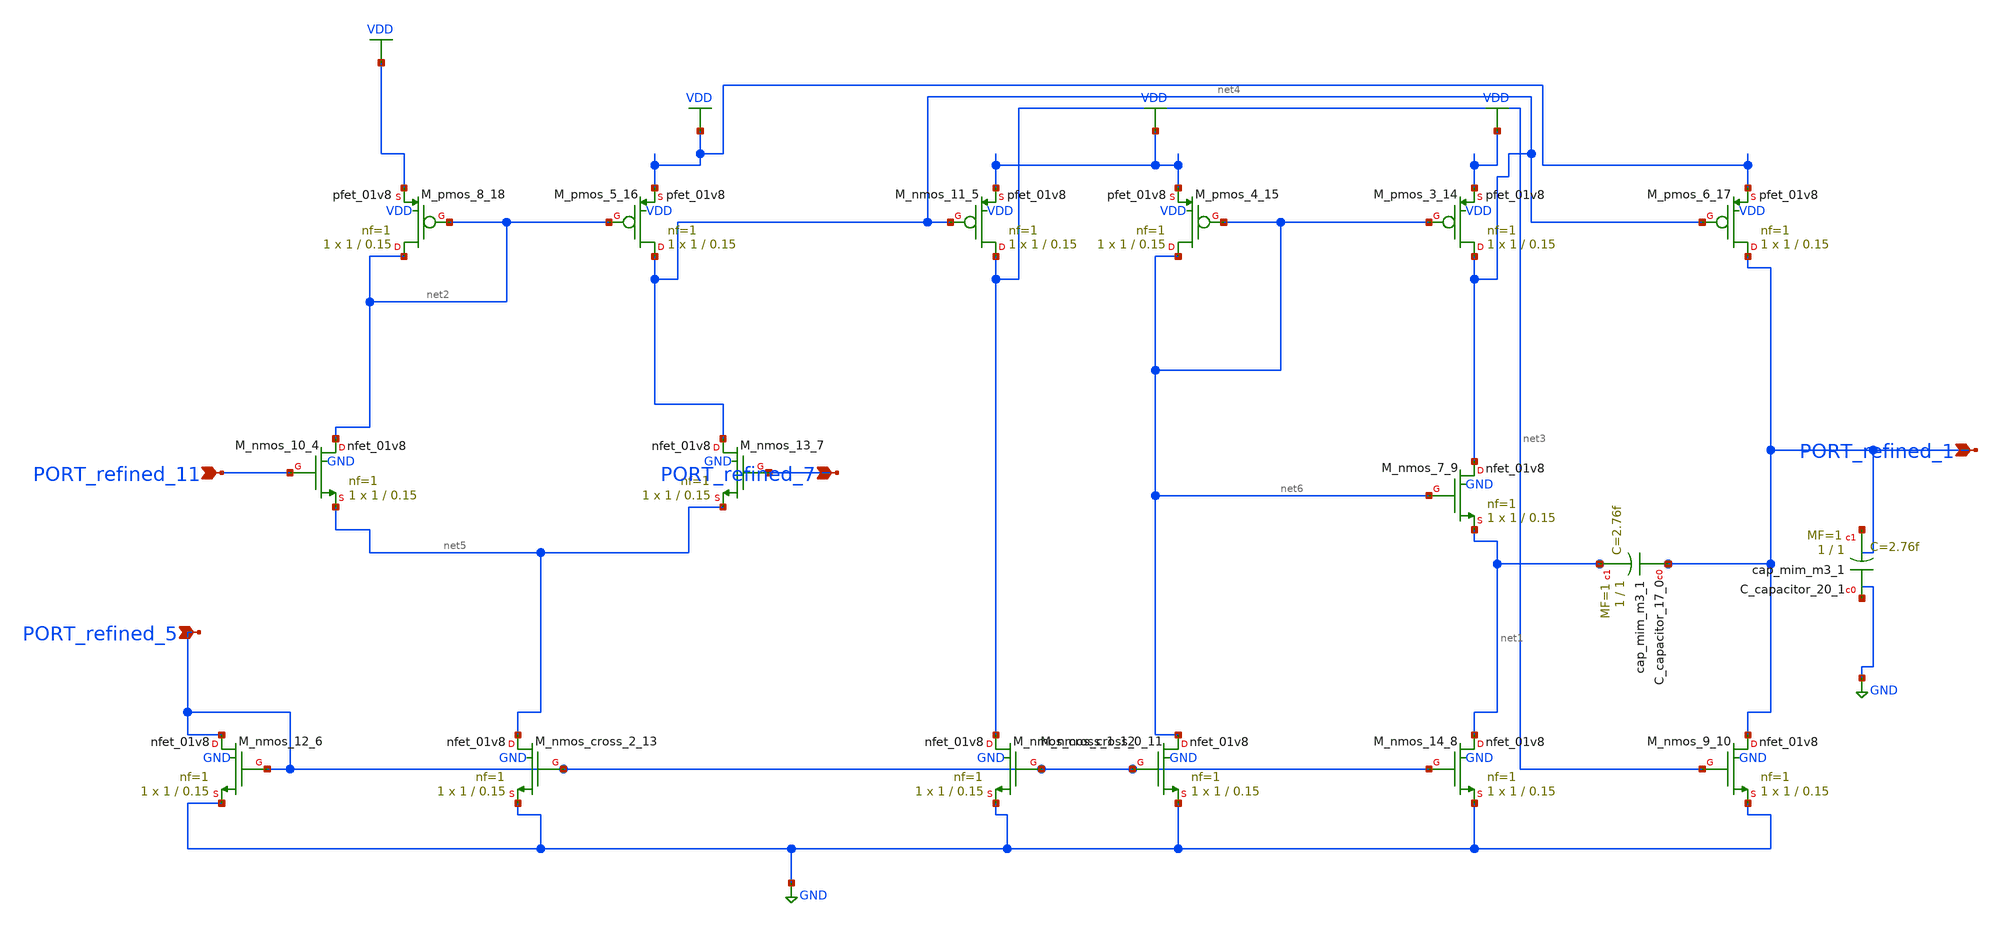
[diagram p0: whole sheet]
** sch_path: schematics/Image2Net/080.sch
**.subckt 080 PORT_refined_7 PORT_refined_11 PORT_refined_1 PORT_refined_5
*.ipin PORT_refined_7
*.ipin PORT_refined_11
*.ipin PORT_refined_1
*.ipin PORT_refined_5
XC_capacitor_17_0 PORT_refined_1 net1 sky130_fd_pr__cap_mim_m3_1 W=1 L=1 MF=1 m=1
XC_capacitor_20_1 GND PORT_refined_1 sky130_fd_pr__cap_mim_m3_1 W=1 L=1 MF=1 m=1
XM_nmos_10_4 net2 PORT_refined_11 net5 GND sky130_fd_pr__nfet_01v8 L=0.15 W=1 nf=1 ad='int((1 + 1)/2) * 1 / 1 * 0.29'
+ as='int((1 + 2)/2) * 1 / 1 * 0.29' pd='2*int((1 + 1)/2) * (1 / 1 + 0.29)' ps='2*int((1 + 2)/2) * (1 / 1 + 0.29)'
+ nrd='0.29 / 1 ' nrs='0.29 / 1 ' sa=0 sb=0 sd=0 mult=1 m=1
XM_nmos_11_5 net3 net4 VDD VDD sky130_fd_pr__pfet_01v8 L=0.15 W=1 nf=1 ad='int((1 + 1)/2) * 1 / 1 * 0.29'
+ as='int((1 + 2)/2) * 1 / 1 * 0.29' pd='2*int((1 + 1)/2) * (1 / 1 + 0.29)' ps='2*int((1 + 2)/2) * (1 / 1 + 0.29)'
+ nrd='0.29 / 1 ' nrs='0.29 / 1 ' sa=0 sb=0 sd=0 mult=1 m=1
XM_nmos_12_6 PORT_refined_5 PORT_refined_5 GND GND sky130_fd_pr__nfet_01v8 L=0.15 W=1 nf=1 ad='int((1 + 1)/2) * 1 / 1 * 0.29'
+ as='int((1 + 2)/2) * 1 / 1 * 0.29' pd='2*int((1 + 1)/2) * (1 / 1 + 0.29)' ps='2*int((1 + 2)/2) * (1 / 1 + 0.29)'
+ nrd='0.29 / 1 ' nrs='0.29 / 1 ' sa=0 sb=0 sd=0 mult=1 m=1
XM_nmos_13_7 net4 PORT_refined_7 net5 GND sky130_fd_pr__nfet_01v8 L=0.15 W=1 nf=1 ad='int((1 + 1)/2) * 1 / 1 * 0.29'
+ as='int((1 + 2)/2) * 1 / 1 * 0.29' pd='2*int((1 + 1)/2) * (1 / 1 + 0.29)' ps='2*int((1 + 2)/2) * (1 / 1 + 0.29)'
+ nrd='0.29 / 1 ' nrs='0.29 / 1 ' sa=0 sb=0 sd=0 mult=1 m=1
XM_nmos_14_8 net1 PORT_refined_5 GND GND sky130_fd_pr__nfet_01v8 L=0.15 W=1 nf=1 ad='int((1 + 1)/2) * 1 / 1 * 0.29'
+ as='int((1 + 2)/2) * 1 / 1 * 0.29' pd='2*int((1 + 1)/2) * (1 / 1 + 0.29)' ps='2*int((1 + 2)/2) * (1 / 1 + 0.29)'
+ nrd='0.29 / 1 ' nrs='0.29 / 1 ' sa=0 sb=0 sd=0 mult=1 m=1
XM_nmos_7_9 net4 net6 net1 GND sky130_fd_pr__nfet_01v8 L=0.15 W=1 nf=1 ad='int((1 + 1)/2) * 1 / 1 * 0.29'
+ as='int((1 + 2)/2) * 1 / 1 * 0.29' pd='2*int((1 + 1)/2) * (1 / 1 + 0.29)' ps='2*int((1 + 2)/2) * (1 / 1 + 0.29)'
+ nrd='0.29 / 1 ' nrs='0.29 / 1 ' sa=0 sb=0 sd=0 mult=1 m=1
XM_nmos_9_10 PORT_refined_1 net3 GND GND sky130_fd_pr__nfet_01v8 L=0.15 W=1 nf=1 ad='int((1 + 1)/2) * 1 / 1 * 0.29'
+ as='int((1 + 2)/2) * 1 / 1 * 0.29' pd='2*int((1 + 1)/2) * (1 / 1 + 0.29)' ps='2*int((1 + 2)/2) * (1 / 1 + 0.29)'
+ nrd='0.29 / 1 ' nrs='0.29 / 1 ' sa=0 sb=0 sd=0 mult=1 m=1
XM_nmos_cross_0_11 net6 PORT_refined_5 GND GND sky130_fd_pr__nfet_01v8 L=0.15 W=1 nf=1 ad='int((1 + 1)/2) * 1 / 1 * 0.29'
+ as='int((1 + 2)/2) * 1 / 1 * 0.29' pd='2*int((1 + 1)/2) * (1 / 1 + 0.29)' ps='2*int((1 + 2)/2) * (1 / 1 + 0.29)'
+ nrd='0.29 / 1 ' nrs='0.29 / 1 ' sa=0 sb=0 sd=0 mult=1 m=1
XM_nmos_cross_1_12 net3 PORT_refined_5 GND GND sky130_fd_pr__nfet_01v8 L=0.15 W=1 nf=1 ad='int((1 + 1)/2) * 1 / 1 * 0.29'
+ as='int((1 + 2)/2) * 1 / 1 * 0.29' pd='2*int((1 + 1)/2) * (1 / 1 + 0.29)' ps='2*int((1 + 2)/2) * (1 / 1 + 0.29)'
+ nrd='0.29 / 1 ' nrs='0.29 / 1 ' sa=0 sb=0 sd=0 mult=1 m=1
XM_nmos_cross_2_13 net5 PORT_refined_5 GND GND sky130_fd_pr__nfet_01v8 L=0.15 W=1 nf=1 ad='int((1 + 1)/2) * 1 / 1 * 0.29'
+ as='int((1 + 2)/2) * 1 / 1 * 0.29' pd='2*int((1 + 1)/2) * (1 / 1 + 0.29)' ps='2*int((1 + 2)/2) * (1 / 1 + 0.29)'
+ nrd='0.29 / 1 ' nrs='0.29 / 1 ' sa=0 sb=0 sd=0 mult=1 m=1
XM_pmos_3_14 net4 net6 VDD VDD sky130_fd_pr__pfet_01v8 L=0.15 W=1 nf=1 ad='int((1 + 1)/2) * 1 / 1 * 0.29'
+ as='int((1 + 2)/2) * 1 / 1 * 0.29' pd='2*int((1 + 1)/2) * (1 / 1 + 0.29)' ps='2*int((1 + 2)/2) * (1 / 1 + 0.29)'
+ nrd='0.29 / 1 ' nrs='0.29 / 1 ' sa=0 sb=0 sd=0 mult=1 m=1
XM_pmos_4_15 net6 net6 VDD VDD sky130_fd_pr__pfet_01v8 L=0.15 W=1 nf=1 ad='int((1 + 1)/2) * 1 / 1 * 0.29'
+ as='int((1 + 2)/2) * 1 / 1 * 0.29' pd='2*int((1 + 1)/2) * (1 / 1 + 0.29)' ps='2*int((1 + 2)/2) * (1 / 1 + 0.29)'
+ nrd='0.29 / 1 ' nrs='0.29 / 1 ' sa=0 sb=0 sd=0 mult=1 m=1
XM_pmos_5_16 net4 net2 VDD VDD sky130_fd_pr__pfet_01v8 L=0.15 W=1 nf=1 ad='int((1 + 1)/2) * 1 / 1 * 0.29'
+ as='int((1 + 2)/2) * 1 / 1 * 0.29' pd='2*int((1 + 1)/2) * (1 / 1 + 0.29)' ps='2*int((1 + 2)/2) * (1 / 1 + 0.29)'
+ nrd='0.29 / 1 ' nrs='0.29 / 1 ' sa=0 sb=0 sd=0 mult=1 m=1
XM_pmos_6_17 PORT_refined_1 net4 VDD VDD sky130_fd_pr__pfet_01v8 L=0.15 W=1 nf=1 ad='int((1 + 1)/2) * 1 / 1 * 0.29'
+ as='int((1 + 2)/2) * 1 / 1 * 0.29' pd='2*int((1 + 1)/2) * (1 / 1 + 0.29)' ps='2*int((1 + 2)/2) * (1 / 1 + 0.29)'
+ nrd='0.29 / 1 ' nrs='0.29 / 1 ' sa=0 sb=0 sd=0 mult=1 m=1
XM_pmos_8_18 net2 net2 VDD VDD sky130_fd_pr__pfet_01v8 L=0.15 W=1 nf=1 ad='int((1 + 1)/2) * 1 / 1 * 0.29'
+ as='int((1 + 2)/2) * 1 / 1 * 0.29' pd='2*int((1 + 1)/2) * (1 / 1 + 0.29)' ps='2*int((1 + 2)/2) * (1 / 1 + 0.29)'
+ nrd='0.29 / 1 ' nrs='0.29 / 1 ' sa=0 sb=0 sd=0 mult=1 m=1
**.ends
.GLOBAL GND
.GLOBAL VDD
.end
